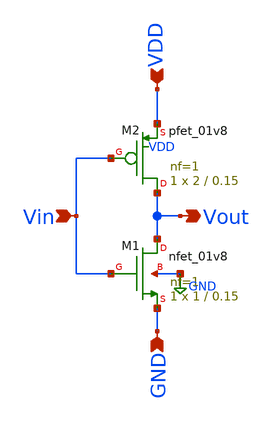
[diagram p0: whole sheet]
** sch_path: Schematics/CMOSInverter.sch
**.subckt CMOSInverter Vin Vout GND VDD
*.ipin Vin
*.opin Vout
*.ipin GND
*.ipin VDD
XM1 Vout Vin GND GND sky130_fd_pr__nfet_01v8 L=0.15 W=1 nf=1 ad='int((nf+1)/2) * W/nf * 0.29' as='int((nf+2)/2) * W/nf * 0.29'
+ pd='2*int((nf+1)/2) * (W/nf + 0.29)' ps='2*int((nf+2)/2) * (W/nf + 0.29)' nrd='0.29 / W' nrs='0.29 / W'
+ sa=0 sb=0 sd=0 mult=1 m=1
XM2 Vout Vin VDD VDD sky130_fd_pr__pfet_01v8 L=0.15 W=2 nf=1 ad='int((nf+1)/2) * W/nf * 0.29' as='int((nf+2)/2) * W/nf * 0.29'
+ pd='2*int((nf+1)/2) * (W/nf + 0.29)' ps='2*int((nf+2)/2) * (W/nf + 0.29)' nrd='0.29 / W' nrs='0.29 / W'
+ sa=0 sb=0 sd=0 mult=1 m=1
**.ends
.GLOBAL GND
.end
